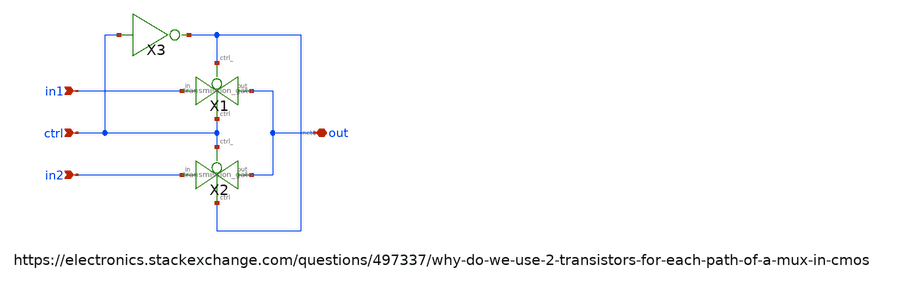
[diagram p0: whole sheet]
** sch_path: xschem/mux/mux2-1.sch
**.subckt mux2-1 in1 ctrl in2 out
*.ipin in1
*.ipin ctrl
*.ipin in2
*.iopin out
X1 in1 out net1 ctrl transmission_gate
X2 in2 out ctrl net1 transmission_gate
X3 ctrl net1 inv
**.ends

* expanding   symbol:  transmission_gate/transmission_gate.sym # of pins=4
** sym_path: xschem/transmission_gate/transmission_gate.sym
** sch_path: xschem/transmission_gate/transmission_gate.sch
.subckt transmission_gate in out ctrl_ ctrl
*.iopin in
*.iopin out
*.ipin ctrl_
*.ipin ctrl
XM3 in ctrl out GND sky130_fd_pr__nfet_01v8 L=0.18 W=1 nf=1 ad='int((nf+1)/2) * W/nf * 0.29' as='int((nf+2)/2) * W/nf * 0.29'
+ pd='2*int((nf+1)/2) * (W/nf + 0.29)' ps='2*int((nf+2)/2) * (W/nf + 0.29)' nrd='0.29 / W' nrs='0.29 / W'
+ sa=0 sb=0 sd=0 mult=1 m=1
XM4 out ctrl_ in VDD sky130_fd_pr__pfet_01v8 L=0.18 W=1 nf=1 ad='int((nf+1)/2) * W/nf * 0.29' as='int((nf+2)/2) * W/nf * 0.29'
+ pd='2*int((nf+1)/2) * (W/nf + 0.29)' ps='2*int((nf+2)/2) * (W/nf + 0.29)' nrd='0.29 / W' nrs='0.29 / W'
+ sa=0 sb=0 sd=0 mult=1 m=1
.ends


* expanding   symbol:  inv/inv.sym # of pins=2
** sym_path: xschem/inv/inv.sym
** sch_path: xschem/inv/inv.sch
.subckt inv in out
*.ipin in
*.iopin out
XM1 out in GND GND sky130_fd_pr__nfet_01v8 L=0.18 W=0.5 nf=1 ad='int((nf+1)/2) * W/nf * 0.29' as='int((nf+2)/2) * W/nf * 0.29'
+ pd='2*int((nf+1)/2) * (W/nf + 0.29)' ps='2*int((nf+2)/2) * (W/nf + 0.29)' nrd='0.29 / W' nrs='0.29 / W'
+ sa=0 sb=0 sd=0 mult=1 m=1
XM2 out in VDD VDD sky130_fd_pr__pfet_01v8 L=0.18 W=1 nf=1 ad='int((nf+1)/2) * W/nf * 0.29' as='int((nf+2)/2) * W/nf * 0.29'
+ pd='2*int((nf+1)/2) * (W/nf + 0.29)' ps='2*int((nf+2)/2) * (W/nf + 0.29)' nrd='0.29 / W' nrs='0.29 / W'
+ sa=0 sb=0 sd=0 mult=1 m=1
.ends

.GLOBAL GND
.GLOBAL VDD
.end
